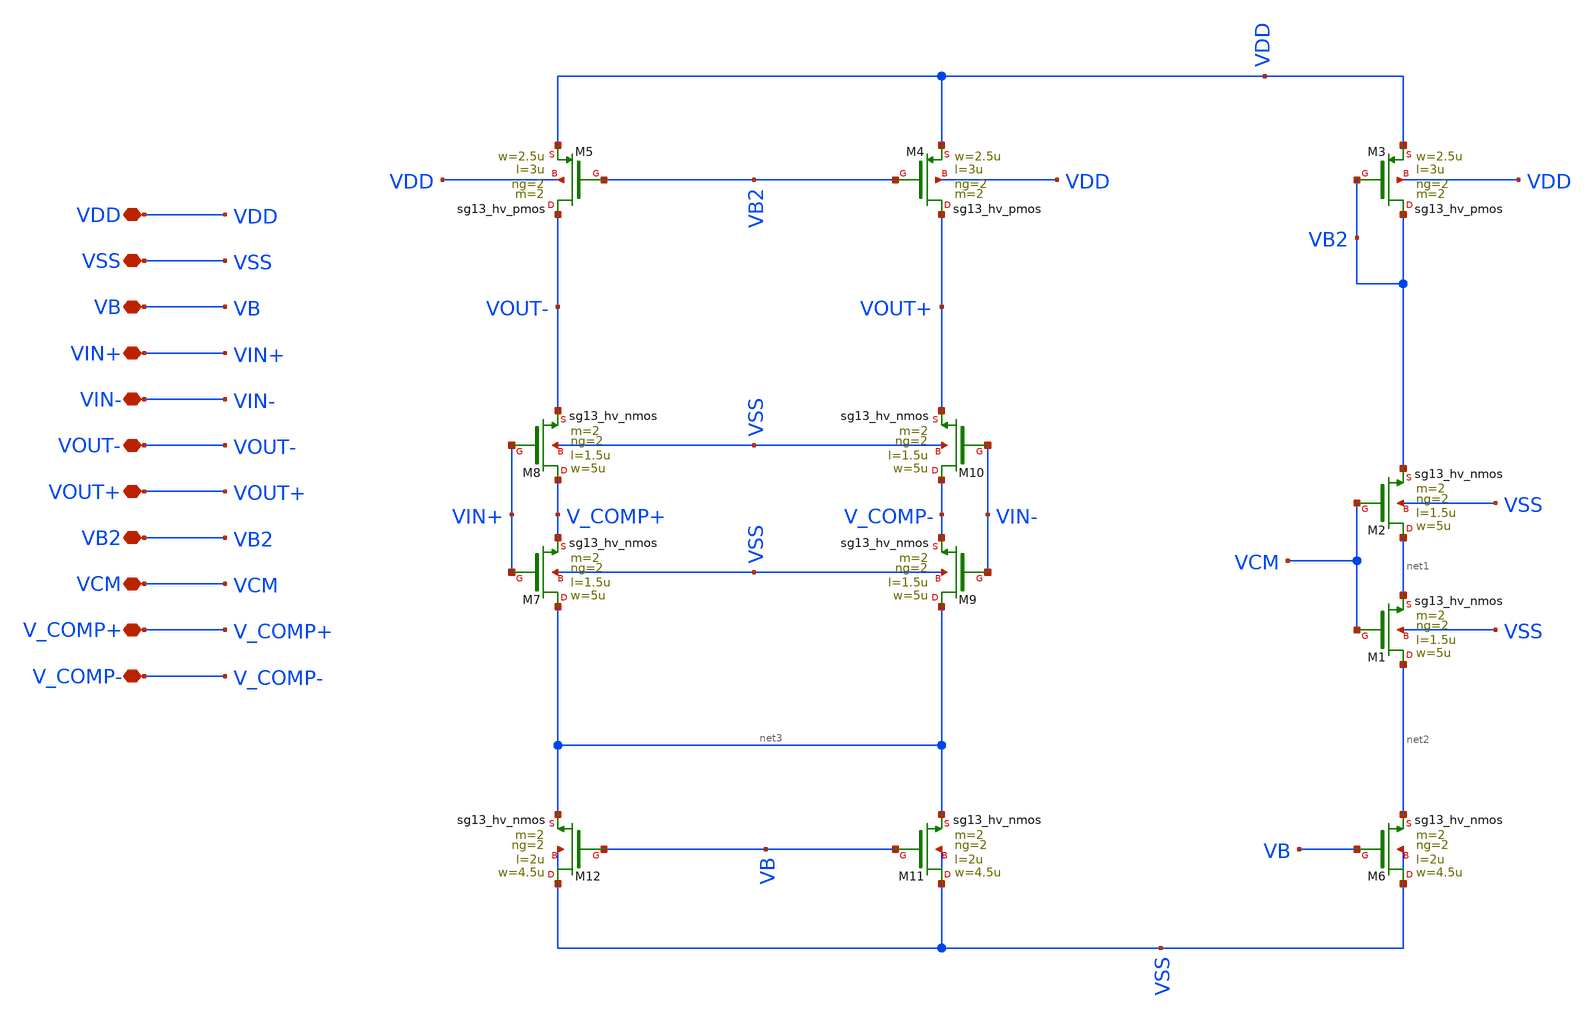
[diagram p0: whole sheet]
** sch_path: my_ip/LIB/ihp-sg13g2/FD_opamp001/first_stage.sch
**.subckt first_stage VDD VSS VB VIN+ VIN- VOUT- VOUT+ VB2 VCM V_COMP+ V_COMP-
*.iopin VDD
*.iopin VSS
*.iopin VB
*.iopin VIN+
*.iopin VIN-
*.iopin VOUT-
*.iopin VOUT+
*.iopin VB2
*.iopin VCM
*.iopin V_COMP+
*.iopin V_COMP-
XM6 VSS VB net2 VSS sg13_hv_nmos w=4.5u l=2u ng=2 m=2 mm_ok=1
XM1 net2 VCM net1 VSS sg13_hv_nmos w=5u l=1.5u ng=2 m=2 mm_ok=1
XM2 net1 VCM VB2 VSS sg13_hv_nmos w=5u l=1.5u ng=2 m=2 mm_ok=1
XM3 VB2 VB2 VDD VDD sg13_hv_pmos w=2.5u l=3u ng=2 m=2 mm_ok=1
XM7 net3 VIN+ V_COMP+ VSS sg13_hv_nmos w=5u l=1.5u ng=2 m=2 mm_ok=1
XM8 V_COMP+ VIN+ VOUT- VSS sg13_hv_nmos w=5u l=1.5u ng=2 m=2 mm_ok=1
XM9 net3 VIN- V_COMP- VSS sg13_hv_nmos w=5u l=1.5u ng=2 m=2 mm_ok=1
XM10 V_COMP- VIN- VOUT+ VSS sg13_hv_nmos w=5u l=1.5u ng=2 m=2 mm_ok=1
XM11 VSS VB net3 VSS sg13_hv_nmos w=4.5u l=2u ng=2 m=2 mm_ok=1
XM12 VSS VB net3 VSS sg13_hv_nmos w=4.5u l=2u ng=2 m=2 mm_ok=1
XM4 VOUT+ VB2 VDD VDD sg13_hv_pmos w=2.5u l=3u ng=2 m=2 mm_ok=1
XM5 VOUT- VB2 VDD VDD sg13_hv_pmos w=2.5u l=3u ng=2 m=2 mm_ok=1
**.ends
.end
